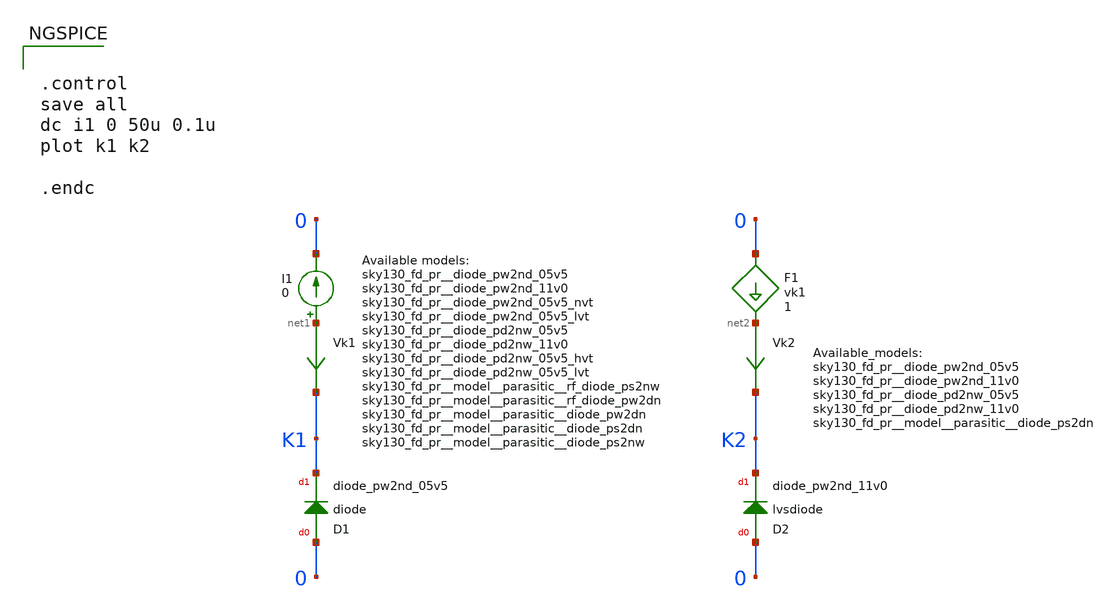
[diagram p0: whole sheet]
** sch_path: sky130_tests/test_diode.sch
* Copyright 2021 Stefan Frederik Schippers
* Licensed under the Apache License, Version 2.0 (the "License");
* you may not use this file except in compliance with the License.
* You may obtain a copy of the License at
* https://www.apache.org/licenses/LICENSE-2.0
* Unless required by applicable law or agreed to in writing, software
* distributed under the License is distributed on an "AS IS" BASIS,
* WITHOUT WARRANTIES OR CONDITIONS OF ANY KIND, either express or implied.
* See the License for the specific language governing permissions and
* limitations under the License.
**.subckt test_diode
I1 net1 0 0
Vk1 net1 K1 0
.save i(vk1)
D1 0 K1 sky130_fd_pr__diode_pw2nd_05v5 area=1
Vk2 net2 K2 0
.save i(vk2)
D2 0 K2 sky130_fd_pr__diode_pw2nd_11v0 area=1
F1 0 net2 vk1 1
**** begin user architecture code


.control
save all
dc i1 0 50u 0.1u
plot k1 k2

.endc


 ** manual skywater pdks install (with patches applied)
* .lib $::SKYWATER_MODELS/models/sky130.lib.spice tt

** opencircuitdesign pdks install
.lib $::SKYWATER_MODELS/sky130.lib.spice tt

.param mc_mm_switch=0
.param mc_pr_switch=0

**** end user architecture code
**.ends
.end
